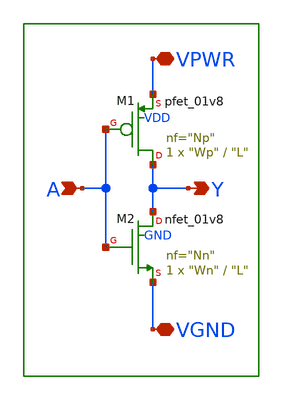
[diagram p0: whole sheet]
** sch_path: circuit_model/lib/inverter.sch
**.subckt inverter VPWR VGND A Y
*.iopin VPWR
*.iopin VGND
*.ipin A
*.opin Y
XM1 Y A VPWR VDD sky130_fd_pr__pfet_01v8 L="L" W="Wp" nf="Np" ad='int(("Np" + 1)/2) * "Wp" / "Np" * 0.29'
+ as='int(("Np" + 2)/2) * "Wp" / "Np" * 0.29' pd='2*int(("Np" + 1)/2) * ("Wp" / "Np" + 0.29)' ps='2*int(("Np" + 2)/2) * ("Wp" / "Np" + 0.29)'
+ nrd='0.29 / "Wp" ' nrs='0.29 / "Wp" ' sa=0 sb=0 sd=0 mult=1 m=1
XM2 Y A VGND GND sky130_fd_pr__nfet_01v8 L="L" W="Wn" nf="Nn" ad='int((nf+1)/2) * W/nf * 0.29' as='int((nf+2)/2) * W/nf * 0.29'
+ pd='2*int((nf+1)/2) * (W/nf + 0.29)' ps='2*int((nf+2)/2) * (W/nf + 0.29)' nrd='0.29 / W' nrs='0.29 / W'
+ sa=0 sb=0 sd=0 mult=1 m=1
**.ends
.end
